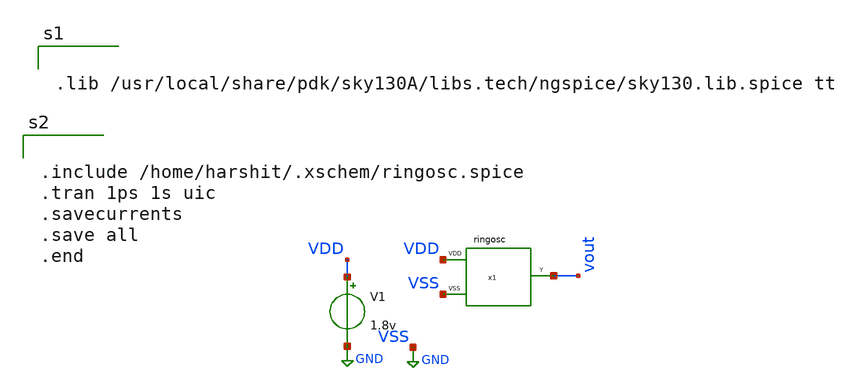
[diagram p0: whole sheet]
** sch_path: xschem files/ringosc_tran.sch
**.subckt ringosc_tran
V1 VDD GND 1.8v
x1 VDD vout VSS ringosc
**** begin user architecture code


.lib /usr/local/share/pdk/sky130A/libs.tech/ngspice/sky130.lib.spice tt



.include /home/harshit/.xschem/ringosc.spice
.tran 1ps 1s uic
.savecurrents
.save all
.end

**** end user architecture code
**.ends
.GLOBAL GND
.end
